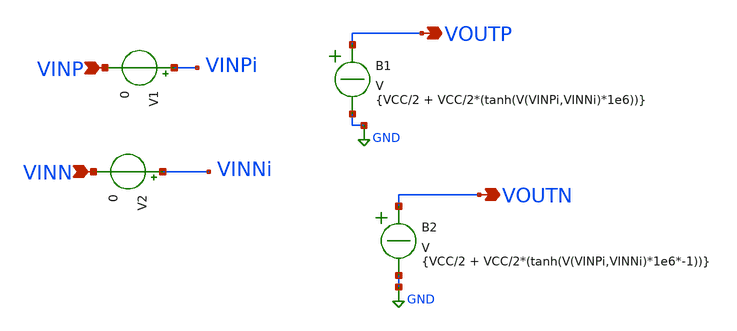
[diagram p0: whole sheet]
** sch_path: comparator_behav.sch
**.subckt comparator_behav VINP VINN VOUTP VOUTN
*.ipin VINP
*.ipin VINN
*.opin VOUTP
*.opin VOUTN
V1 VINPi VINP 0
V2 VINNi VINN 0
B1 VOUTP GND V = {VCC/2 + VCC/2*(tanh(V(VINPi,VINNi)*1e6))}
B2 VOUTN GND V = {VCC/2 + VCC/2*(tanh(V(VINPi,VINNi)*1e6*-1))}
**.ends
.GLOBAL GND
.end
